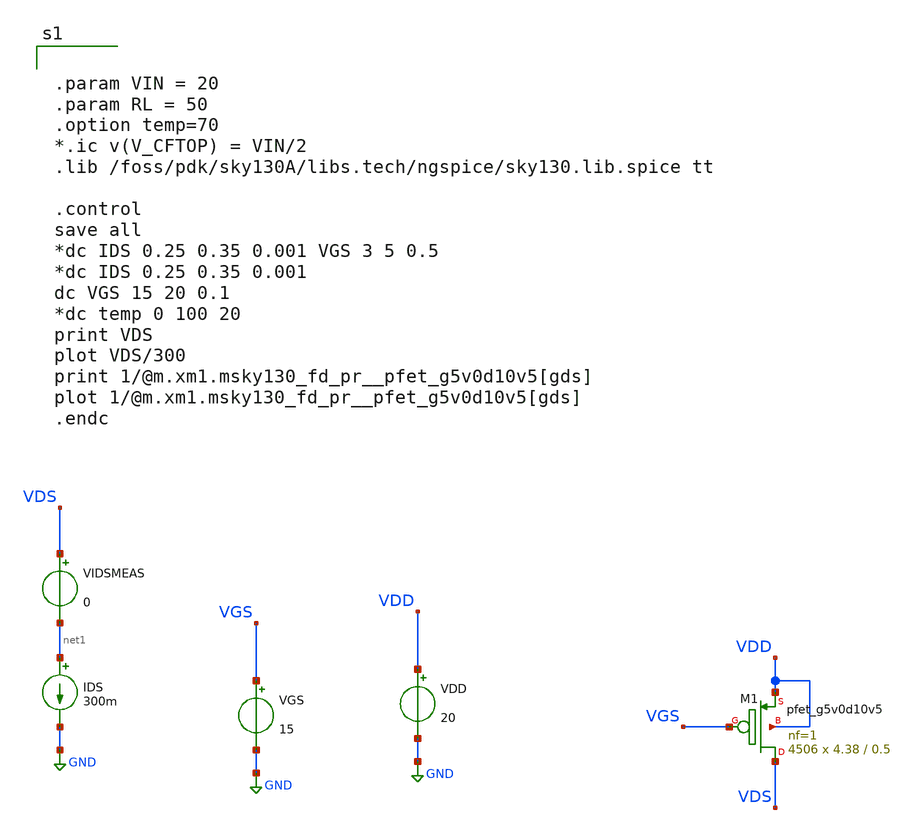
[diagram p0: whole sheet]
** sch_path: xschem/dev_switches/PMOS_allfingers_RONcalc_v2p2_tomas.sch
**.subckt PMOS_allfingers_RONcalc_v2p2_tomas
VGS VGS GND 15
IDS net1 GND 300m
VIDSMEAS VDS net1 0
XM1 VDS VGS VDD VDD sky130_fd_pr__pfet_g5v0d10v5 L=0.5 W=4.38 nf=1 ad='int((nf+1)/2) * W/nf * 0.29' as='int((nf+2)/2) * W/nf * 0.29'
+ pd='2*int((nf+1)/2) * (W/nf + 0.29)' ps='2*int((nf+2)/2) * (W/nf + 0.29)' nrd='0.29 / W' nrs='0.29 / W'
+ sa=0 sb=0 sd=0 mult=4506 m=4506
VDD VDD GND 20
**** begin user architecture code


.param VIN = 20
.param RL = 50
.option temp=70
*.ic v(V_CFTOP) = VIN/2
.lib /foss/pdk/sky130A/libs.tech/ngspice/sky130.lib.spice tt

.control
save all
*dc IDS 0.25 0.35 0.001 VGS 3 5 0.5
*dc IDS 0.25 0.35 0.001
dc VGS 15 20 0.1
*dc temp 0 100 20
print VDS
plot VDS/300
print 1/@m.xm1.msky130_fd_pr__pfet_g5v0d10v5[gds]
plot 1/@m.xm1.msky130_fd_pr__pfet_g5v0d10v5[gds]
.endc


**** end user architecture code
**.ends
.GLOBAL GND
.end
